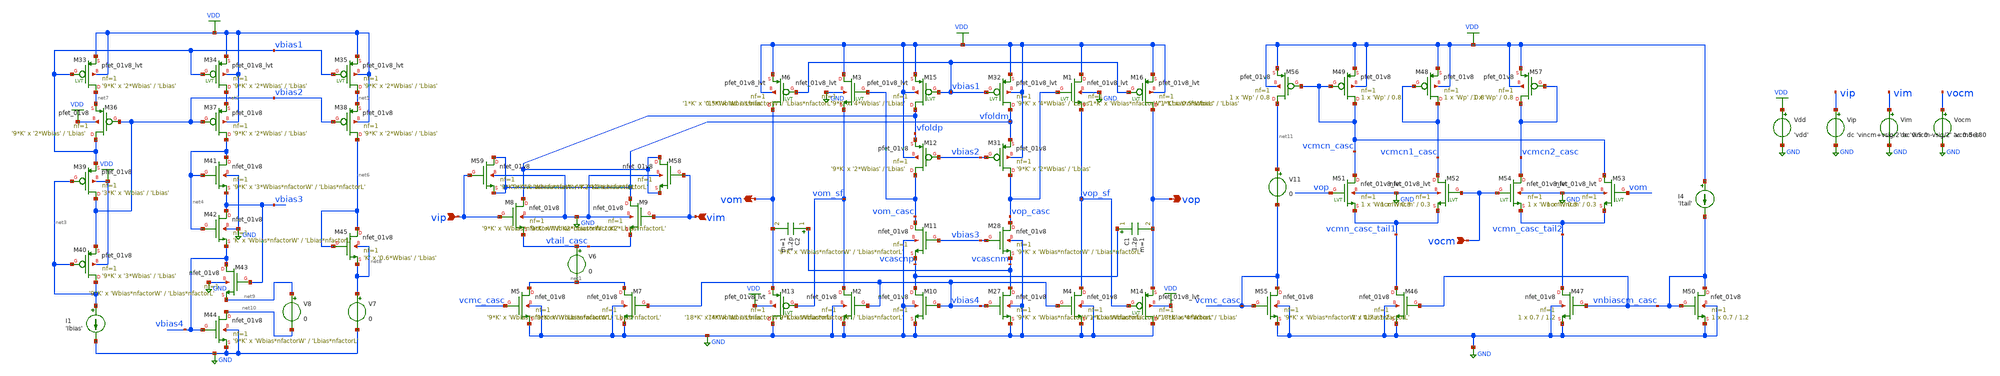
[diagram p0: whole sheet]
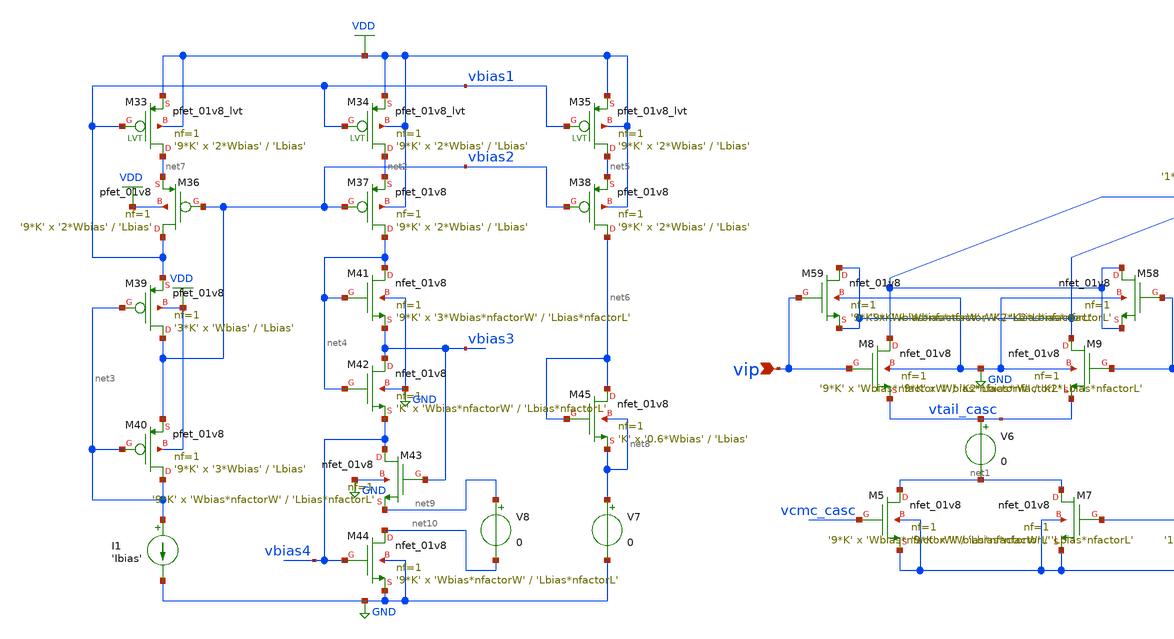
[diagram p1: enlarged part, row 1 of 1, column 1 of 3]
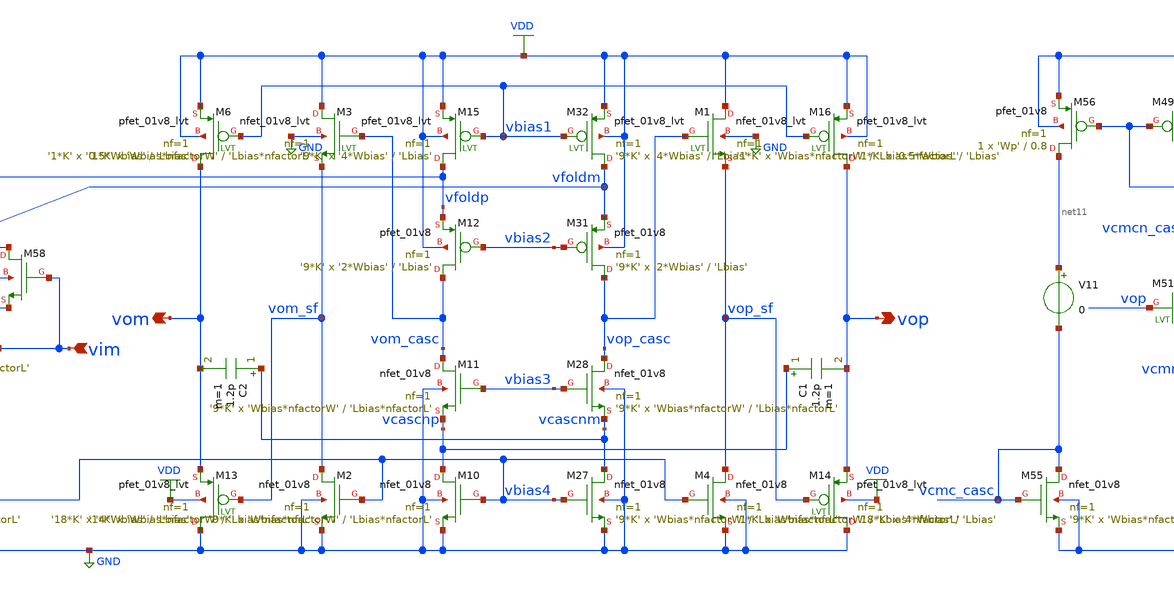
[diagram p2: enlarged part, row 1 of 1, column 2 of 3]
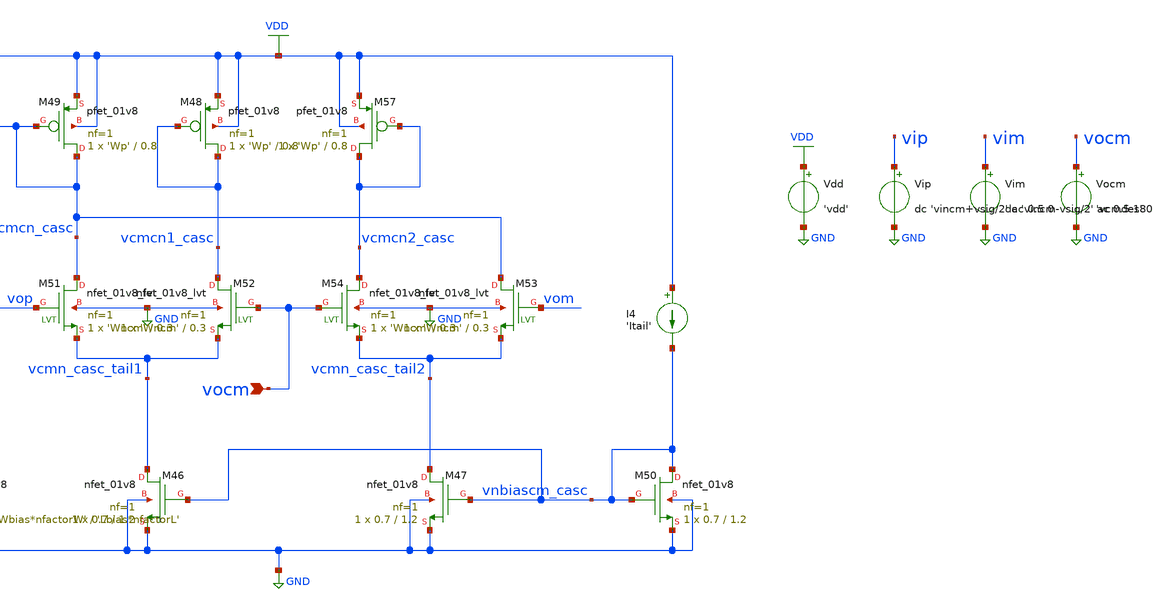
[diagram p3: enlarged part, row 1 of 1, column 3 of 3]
** sch_path: designs/diff_fold_casc_opamp.sch
* Copyright 2020 Stefan Frederik Schippers
* Licensed under the Apache License, Version 2.0 (the "License");
* you may not use this file except in compliance with the License.
* You may obtain a copy of the License at
* https://www.apache.org/licenses/LICENSE-2.0
* Unless required by applicable law or agreed to in writing, software
* distributed under the License is distributed on an "AS IS" BASIS,
* WITHOUT WARRANTIES OR CONDITIONS OF ANY KIND, either express or implied.
* See the License for the specific language governing permissions and
* limitations under the License.
**.subckt diff_fold_casc_opamp vip vim vocm vom vop
*.ipin vip
*.ipin vim
*.ipin vocm
*.opin vom
*.opin vop
Vdd VDD GND 'vdd'
V6 vtail_casc net1 0
XM7 net1 vbias4 GND GND sky130_fd_pr__nfet_01v8 L='Lbias*nfactorL' W='Wbias*nfactorW' nf=1 ad='int((nf+1)/2) * W/nf * 0.29'
+ as='int((nf+2)/2) * W/nf * 0.29' pd='2*int((nf+1)/2) * (W/nf + 0.29)' ps='2*int((nf+2)/2) * (W/nf + 0.29)'
+ nrd='0.29 / W' nrs='0.29 / W' sa=0 sb=0 sd=0 mult='9*K' m='9*K'
XM10 vcascnp vbias4 GND GND sky130_fd_pr__nfet_01v8 L='Lbias*nfactorL' W='Wbias*nfactorW' nf=1 ad='int((nf+1)/2) * W/nf * 0.29'
+ as='int((nf+2)/2) * W/nf * 0.29' pd='2*int((nf+1)/2) * (W/nf + 0.29)' ps='2*int((nf+2)/2) * (W/nf + 0.29)'
+ nrd='0.29 / W' nrs='0.29 / W' sa=0 sb=0 sd=0 mult='9*K' m='9*K'
XM11 vom_casc vbias3 vcascnp GND sky130_fd_pr__nfet_01v8 L='Lbias*nfactorL' W='Wbias*nfactorW' nf=1 ad='int((nf+1)/2) * W/nf * 0.29'
+ as='int((nf+2)/2) * W/nf * 0.29' pd='2*int((nf+1)/2) * (W/nf + 0.29)' ps='2*int((nf+2)/2) * (W/nf + 0.29)'
+ nrd='0.29 / W' nrs='0.29 / W' sa=0 sb=0 sd=0 mult='9*K' m='9*K'
XM27 vcascnm vbias4 GND GND sky130_fd_pr__nfet_01v8 L='Lbias*nfactorL' W='Wbias*nfactorW' nf=1 ad='int((nf+1)/2) * W/nf * 0.29'
+ as='int((nf+2)/2) * W/nf * 0.29' pd='2*int((nf+1)/2) * (W/nf + 0.29)' ps='2*int((nf+2)/2) * (W/nf + 0.29)'
+ nrd='0.29 / W' nrs='0.29 / W' sa=0 sb=0 sd=0 mult='9*K' m='9*K'
XM28 vop_casc vbias3 vcascnm GND sky130_fd_pr__nfet_01v8 L='Lbias*nfactorL' W='Wbias*nfactorW' nf=1 ad='int((nf+1)/2) * W/nf * 0.29'
+ as='int((nf+2)/2) * W/nf * 0.29' pd='2*int((nf+1)/2) * (W/nf + 0.29)' ps='2*int((nf+2)/2) * (W/nf + 0.29)'
+ nrd='0.29 / W' nrs='0.29 / W' sa=0 sb=0 sd=0 mult='9*K' m='9*K'
XM36 vbias1 vbias2 net7 VDD sky130_fd_pr__pfet_01v8 L='Lbias' W='2*Wbias' nf=1 ad='int((nf+1)/2) * W/nf * 0.29'
+ as='int((nf+2)/2) * W/nf * 0.29' pd='2*int((nf+1)/2) * (W/nf + 0.29)' ps='2*int((nf+2)/2) * (W/nf + 0.29)'
+ nrd='0.29 / W' nrs='0.29 / W' sa=0 sb=0 sd=0 mult='9*K' m='9*K'
XM37 net4 vbias2 net2 VDD sky130_fd_pr__pfet_01v8 L='Lbias' W='2*Wbias' nf=1 ad='int((nf+1)/2) * W/nf * 0.29'
+ as='int((nf+2)/2) * W/nf * 0.29' pd='2*int((nf+1)/2) * (W/nf + 0.29)' ps='2*int((nf+2)/2) * (W/nf + 0.29)'
+ nrd='0.29 / W' nrs='0.29 / W' sa=0 sb=0 sd=0 mult='9*K' m='9*K'
XM38 net6 vbias2 net5 VDD sky130_fd_pr__pfet_01v8 L='Lbias' W='2*Wbias' nf=1 ad='int((nf+1)/2) * W/nf * 0.29'
+ as='int((nf+2)/2) * W/nf * 0.29' pd='2*int((nf+1)/2) * (W/nf + 0.29)' ps='2*int((nf+2)/2) * (W/nf + 0.29)'
+ nrd='0.29 / W' nrs='0.29 / W' sa=0 sb=0 sd=0 mult='9*K' m='9*K'
XM39 vbias2 net3 vbias1 VDD sky130_fd_pr__pfet_01v8 L='Lbias' W='Wbias' nf=1 ad='int((nf+1)/2) * W/nf * 0.29'
+ as='int((nf+2)/2) * W/nf * 0.29' pd='2*int((nf+1)/2) * (W/nf + 0.29)' ps='2*int((nf+2)/2) * (W/nf + 0.29)'
+ nrd='0.29 / W' nrs='0.29 / W' sa=0 sb=0 sd=0 mult='3*K' m='3*K'
XM40 net3 net3 vbias2 VDD sky130_fd_pr__pfet_01v8 L='Lbias' W='3*Wbias' nf=1 ad='int((nf+1)/2) * W/nf * 0.29'
+ as='int((nf+2)/2) * W/nf * 0.29' pd='2*int((nf+1)/2) * (W/nf + 0.29)' ps='2*int((nf+2)/2) * (W/nf + 0.29)'
+ nrd='0.29 / W' nrs='0.29 / W' sa=0 sb=0 sd=0 mult='9*K' m='9*K'
XM41 net4 net4 vbias3 GND sky130_fd_pr__nfet_01v8 L='Lbias*nfactorL' W='3*Wbias*nfactorW' nf=1 ad='int((nf+1)/2) * W/nf * 0.29'
+ as='int((nf+2)/2) * W/nf * 0.29' pd='2*int((nf+1)/2) * (W/nf + 0.29)' ps='2*int((nf+2)/2) * (W/nf + 0.29)'
+ nrd='0.29 / W' nrs='0.29 / W' sa=0 sb=0 sd=0 mult='9*K' m='9*K'
XM42 vbias3 net4 vbias4 GND sky130_fd_pr__nfet_01v8 L='Lbias*nfactorL' W='Wbias*nfactorW' nf=1 ad='int((nf+1)/2) * W/nf * 0.29'
+ as='int((nf+2)/2) * W/nf * 0.29' pd='2*int((nf+1)/2) * (W/nf + 0.29)' ps='2*int((nf+2)/2) * (W/nf + 0.29)'
+ nrd='0.29 / W' nrs='0.29 / W' sa=0 sb=0 sd=0 mult='K' m='K'
XM43 vbias4 vbias3 net9 GND sky130_fd_pr__nfet_01v8 L='Lbias*nfactorL' W='Wbias*nfactorW' nf=1 ad='int((nf+1)/2) * W/nf * 0.29'
+ as='int((nf+2)/2) * W/nf * 0.29' pd='2*int((nf+1)/2) * (W/nf + 0.29)' ps='2*int((nf+2)/2) * (W/nf + 0.29)'
+ nrd='0.29 / W' nrs='0.29 / W' sa=0 sb=0 sd=0 mult='9*K' m='9*K'
XM44 net10 vbias4 GND GND sky130_fd_pr__nfet_01v8 L='Lbias*nfactorL' W='Wbias*nfactorW' nf=1 ad='int((nf+1)/2) * W/nf * 0.29'
+ as='int((nf+2)/2) * W/nf * 0.29' pd='2*int((nf+1)/2) * (W/nf + 0.29)' ps='2*int((nf+2)/2) * (W/nf + 0.29)'
+ nrd='0.29 / W' nrs='0.29 / W' sa=0 sb=0 sd=0 mult='9*K' m='9*K'
XM45 net6 net6 net8 net8 sky130_fd_pr__nfet_01v8 L='Lbias' W='0.6*Wbias' nf=1 ad='int((nf+1)/2) * W/nf * 0.29'
+ as='int((nf+2)/2) * W/nf * 0.29' pd='2*int((nf+1)/2) * (W/nf + 0.29)' ps='2*int((nf+2)/2) * (W/nf + 0.29)'
+ nrd='0.29 / W' nrs='0.29 / W' sa=0 sb=0 sd=0 mult='K' m='K'
I1 net3 GND 'Ibias'
V7 net8 GND 0
V8 net9 net10 0
XM8 vfoldp vip vtail_casc GND sky130_fd_pr__nfet_01v8 L='K2*Lbias*nfactorL' W='Wbias*nfactorW' nf=1 ad='int((nf+1)/2) * W/nf * 0.29'
+ as='int((nf+2)/2) * W/nf * 0.29' pd='2*int((nf+1)/2) * (W/nf + 0.29)' ps='2*int((nf+2)/2) * (W/nf + 0.29)'
+ nrd='0.29 / W' nrs='0.29 / W' sa=0 sb=0 sd=0 mult='9*K' m='9*K'
Vip vip GND dc 'vincm+vsig/2' ac 0.5 0
Vim vim GND dc 'vincm-vsig/2' ac 0.5 180
XM46 vcmn_casc_tail1 vnbiascm_casc GND GND sky130_fd_pr__nfet_01v8 L=1.2 W=0.7 nf=1 ad='int((nf+1)/2) * W/nf * 0.29'
+ as='int((nf+2)/2) * W/nf * 0.29' pd='2*int((nf+1)/2) * (W/nf + 0.29)' ps='2*int((nf+2)/2) * (W/nf + 0.29)'
+ nrd='0.29 / W' nrs='0.29 / W' sa=0 sb=0 sd=0 mult=1 m=1
XM47 vcmn_casc_tail2 vnbiascm_casc GND GND sky130_fd_pr__nfet_01v8 L=1.2 W=0.7 nf=1 ad='int((nf+1)/2) * W/nf * 0.29'
+ as='int((nf+2)/2) * W/nf * 0.29' pd='2*int((nf+1)/2) * (W/nf + 0.29)' ps='2*int((nf+2)/2) * (W/nf + 0.29)'
+ nrd='0.29 / W' nrs='0.29 / W' sa=0 sb=0 sd=0 mult=1 m=1
XM48 vcmcn1_casc vcmcn1_casc VDD VDD sky130_fd_pr__pfet_01v8 L=0.8 W='Wp' nf=1 ad='int((nf+1)/2) * W/nf * 0.29'
+ as='int((nf+2)/2) * W/nf * 0.29' pd='2*int((nf+1)/2) * (W/nf + 0.29)' ps='2*int((nf+2)/2) * (W/nf + 0.29)'
+ nrd='0.29 / W' nrs='0.29 / W' sa=0 sb=0 sd=0 mult=1 m=1
XM49 vcmcn_casc vcmcn_casc VDD VDD sky130_fd_pr__pfet_01v8 L=0.8 W='Wp' nf=1 ad='int((nf+1)/2) * W/nf * 0.29'
+ as='int((nf+2)/2) * W/nf * 0.29' pd='2*int((nf+1)/2) * (W/nf + 0.29)' ps='2*int((nf+2)/2) * (W/nf + 0.29)'
+ nrd='0.29 / W' nrs='0.29 / W' sa=0 sb=0 sd=0 mult=1 m=1
I4 VDD vnbiascm_casc 'Itail'
XM50 vnbiascm_casc vnbiascm_casc GND GND sky130_fd_pr__nfet_01v8 L=1.2 W=0.7 nf=1 ad='int((nf+1)/2) * W/nf * 0.29'
+ as='int((nf+2)/2) * W/nf * 0.29' pd='2*int((nf+1)/2) * (W/nf + 0.29)' ps='2*int((nf+2)/2) * (W/nf + 0.29)'
+ nrd='0.29 / W' nrs='0.29 / W' sa=0 sb=0 sd=0 mult=1 m=1
XM51 vcmcn_casc vop vcmn_casc_tail1 GND sky130_fd_pr__nfet_01v8_lvt L=0.3 W='Wncm' nf=1 ad='int((nf+1)/2) * W/nf * 0.29'
+ as='int((nf+2)/2) * W/nf * 0.29' pd='2*int((nf+1)/2) * (W/nf + 0.29)' ps='2*int((nf+2)/2) * (W/nf + 0.29)'
+ nrd='0.29 / W' nrs='0.29 / W' sa=0 sb=0 sd=0 mult=1 m=1
XM52 vcmcn1_casc vocm vcmn_casc_tail1 GND sky130_fd_pr__nfet_01v8_lvt L=0.3 W='Wncm' nf=1 ad='int((nf+1)/2) * W/nf * 0.29'
+ as='int((nf+2)/2) * W/nf * 0.29' pd='2*int((nf+1)/2) * (W/nf + 0.29)' ps='2*int((nf+2)/2) * (W/nf + 0.29)'
+ nrd='0.29 / W' nrs='0.29 / W' sa=0 sb=0 sd=0 mult=1 m=1
XM53 vcmcn_casc vom vcmn_casc_tail2 GND sky130_fd_pr__nfet_01v8_lvt L=0.3 W='Wncm' nf=1 ad='int((nf+1)/2) * W/nf * 0.29'
+ as='int((nf+2)/2) * W/nf * 0.29' pd='2*int((nf+1)/2) * (W/nf + 0.29)' ps='2*int((nf+2)/2) * (W/nf + 0.29)'
+ nrd='0.29 / W' nrs='0.29 / W' sa=0 sb=0 sd=0 mult=1 m=1
XM54 vcmcn2_casc vocm vcmn_casc_tail2 GND sky130_fd_pr__nfet_01v8_lvt L=0.3 W='Wncm' nf=1 ad='int((nf+1)/2) * W/nf * 0.29'
+ as='int((nf+2)/2) * W/nf * 0.29' pd='2*int((nf+1)/2) * (W/nf + 0.29)' ps='2*int((nf+2)/2) * (W/nf + 0.29)'
+ nrd='0.29 / W' nrs='0.29 / W' sa=0 sb=0 sd=0 mult=1 m=1
XM56 net11 vcmcn_casc VDD VDD sky130_fd_pr__pfet_01v8 L=0.8 W='Wp' nf=1 ad='int((nf+1)/2) * W/nf * 0.29'
+ as='int((nf+2)/2) * W/nf * 0.29' pd='2*int((nf+1)/2) * (W/nf + 0.29)' ps='2*int((nf+2)/2) * (W/nf + 0.29)'
+ nrd='0.29 / W' nrs='0.29 / W' sa=0 sb=0 sd=0 mult=1 m=1
XM57 vcmcn2_casc vcmcn2_casc VDD VDD sky130_fd_pr__pfet_01v8 L=0.8 W='Wp' nf=1 ad='int((nf+1)/2) * W/nf * 0.29'
+ as='int((nf+2)/2) * W/nf * 0.29' pd='2*int((nf+1)/2) * (W/nf + 0.29)' ps='2*int((nf+2)/2) * (W/nf + 0.29)'
+ nrd='0.29 / W' nrs='0.29 / W' sa=0 sb=0 sd=0 mult=1 m=1
V11 net11 vcmc_casc 0
Vocm vocm GND 'vcmdes'
XM12 vom_casc vbias2 vfoldp VDD sky130_fd_pr__pfet_01v8 L='Lbias' W='2*Wbias' nf=1 ad='int((nf+1)/2) * W/nf * 0.29'
+ as='int((nf+2)/2) * W/nf * 0.29' pd='2*int((nf+1)/2) * (W/nf + 0.29)' ps='2*int((nf+2)/2) * (W/nf + 0.29)'
+ nrd='0.29 / W' nrs='0.29 / W' sa=0 sb=0 sd=0 mult='9*K' m='9*K'
XM31 vop_casc vbias2 vfoldm VDD sky130_fd_pr__pfet_01v8 L='Lbias' W='2*Wbias' nf=1 ad='int((nf+1)/2) * W/nf * 0.29'
+ as='int((nf+2)/2) * W/nf * 0.29' pd='2*int((nf+1)/2) * (W/nf + 0.29)' ps='2*int((nf+2)/2) * (W/nf + 0.29)'
+ nrd='0.29 / W' nrs='0.29 / W' sa=0 sb=0 sd=0 mult='9*K' m='9*K'
XM15 vfoldp vbias1 VDD VDD sky130_fd_pr__pfet_01v8_lvt L='Lbias' W='4*Wbias' nf=1 ad='int((nf+1)/2) * W/nf * 0.29'
+ as='int((nf+2)/2) * W/nf * 0.29' pd='2*int((nf+1)/2) * (W/nf + 0.29)' ps='2*int((nf+2)/2) * (W/nf + 0.29)'
+ nrd='0.29 / W' nrs='0.29 / W' sa=0 sb=0 sd=0 mult='9*K' m='9*K'
XM32 vfoldm vbias1 VDD VDD sky130_fd_pr__pfet_01v8_lvt L='Lbias' W='4*Wbias' nf=1 ad='int((nf+1)/2) * W/nf * 0.29'
+ as='int((nf+2)/2) * W/nf * 0.29' pd='2*int((nf+1)/2) * (W/nf + 0.29)' ps='2*int((nf+2)/2) * (W/nf + 0.29)'
+ nrd='0.29 / W' nrs='0.29 / W' sa=0 sb=0 sd=0 mult='9*K' m='9*K'
XM33 net7 vbias1 VDD VDD sky130_fd_pr__pfet_01v8_lvt L='Lbias' W='2*Wbias' nf=1 ad='int((nf+1)/2) * W/nf * 0.29'
+ as='int((nf+2)/2) * W/nf * 0.29' pd='2*int((nf+1)/2) * (W/nf + 0.29)' ps='2*int((nf+2)/2) * (W/nf + 0.29)'
+ nrd='0.29 / W' nrs='0.29 / W' sa=0 sb=0 sd=0 mult='9*K' m='9*K'
XM34 net2 vbias1 VDD VDD sky130_fd_pr__pfet_01v8_lvt L='Lbias' W='2*Wbias' nf=1 ad='int((nf+1)/2) * W/nf * 0.29'
+ as='int((nf+2)/2) * W/nf * 0.29' pd='2*int((nf+1)/2) * (W/nf + 0.29)' ps='2*int((nf+2)/2) * (W/nf + 0.29)'
+ nrd='0.29 / W' nrs='0.29 / W' sa=0 sb=0 sd=0 mult='9*K' m='9*K'
XM35 net5 vbias1 VDD VDD sky130_fd_pr__pfet_01v8_lvt L='Lbias' W='2*Wbias' nf=1 ad='int((nf+1)/2) * W/nf * 0.29'
+ as='int((nf+2)/2) * W/nf * 0.29' pd='2*int((nf+1)/2) * (W/nf + 0.29)' ps='2*int((nf+2)/2) * (W/nf + 0.29)'
+ nrd='0.29 / W' nrs='0.29 / W' sa=0 sb=0 sd=0 mult='9*K' m='9*K'
XM5 net1 vcmc_casc GND GND sky130_fd_pr__nfet_01v8 L='Lbias*nfactorL' W='Wbias*nfactorW' nf=1 ad='int((nf+1)/2) * W/nf * 0.29'
+ as='int((nf+2)/2) * W/nf * 0.29' pd='2*int((nf+1)/2) * (W/nf + 0.29)' ps='2*int((nf+2)/2) * (W/nf + 0.29)'
+ nrd='0.29 / W' nrs='0.29 / W' sa=0 sb=0 sd=0 mult='9*K' m='9*K'
XM9 vfoldm vim vtail_casc GND sky130_fd_pr__nfet_01v8 L='K2*Lbias*nfactorL' W='Wbias*nfactorW' nf=1 ad='int((nf+1)/2) * W/nf * 0.29'
+ as='int((nf+2)/2) * W/nf * 0.29' pd='2*int((nf+1)/2) * (W/nf + 0.29)' ps='2*int((nf+2)/2) * (W/nf + 0.29)'
+ nrd='0.29 / W' nrs='0.29 / W' sa=0 sb=0 sd=0 mult='9*K' m='9*K'
XM55 vcmc_casc vcmc_casc GND GND sky130_fd_pr__nfet_01v8 L='Lbias*nfactorL' W='Wbias*nfactorW' nf=1 ad='int((nf+1)/2) * W/nf * 0.29'
+ as='int((nf+2)/2) * W/nf * 0.29' pd='2*int((nf+1)/2) * (W/nf + 0.29)' ps='2*int((nf+2)/2) * (W/nf + 0.29)'
+ nrd='0.29 / W' nrs='0.29 / W' sa=0 sb=0 sd=0 mult='9*K' m='9*K'
XM58 vfoldp vim vfoldp GND sky130_fd_pr__nfet_01v8 L='K2*Lbias*nfactorL' W='Wbias*nfactorW' nf=1 ad='int((nf+1)/2) * W/nf * 0.29'
+ as='int((nf+2)/2) * W/nf * 0.29' pd='2*int((nf+1)/2) * (W/nf + 0.29)' ps='2*int((nf+2)/2) * (W/nf + 0.29)'
+ nrd='0.29 / W' nrs='0.29 / W' sa=0 sb=0 sd=0 mult='9*K' m='9*K'
XM59 vfoldm vip vfoldm GND sky130_fd_pr__nfet_01v8 L='K2*Lbias*nfactorL' W='Wbias*nfactorW' nf=1 ad='int((nf+1)/2) * W/nf * 0.29'
+ as='int((nf+2)/2) * W/nf * 0.29' pd='2*int((nf+1)/2) * (W/nf + 0.29)' ps='2*int((nf+2)/2) * (W/nf + 0.29)'
+ nrd='0.29 / W' nrs='0.29 / W' sa=0 sb=0 sd=0 mult='9*K' m='9*K'
XM2 vom_sf vbias4 GND GND sky130_fd_pr__nfet_01v8 L='Lbias*nfactorL' W='Wbias*nfactorW' nf=1 ad='int((nf+1)/2) * W/nf * 0.29'
+ as='int((nf+2)/2) * W/nf * 0.29' pd='2*int((nf+1)/2) * (W/nf + 0.29)' ps='2*int((nf+2)/2) * (W/nf + 0.29)'
+ nrd='0.29 / W' nrs='0.29 / W' sa=0 sb=0 sd=0 mult='1*K' m='1*K'
XM4 vop_sf vbias4 GND GND sky130_fd_pr__nfet_01v8 L='Lbias*nfactorL' W='Wbias*nfactorW' nf=1 ad='int((nf+1)/2) * W/nf * 0.29'
+ as='int((nf+2)/2) * W/nf * 0.29' pd='2*int((nf+1)/2) * (W/nf + 0.29)' ps='2*int((nf+2)/2) * (W/nf + 0.29)'
+ nrd='0.29 / W' nrs='0.29 / W' sa=0 sb=0 sd=0 mult='1*K' m='1*K'
XM1 VDD vop_casc vop_sf GND sky130_fd_pr__nfet_01v8_lvt L='Lbias*nfactorL' W='Wbias*nfactorW' nf=1 ad='int((nf+1)/2) * W/nf * 0.29'
+ as='int((nf+2)/2) * W/nf * 0.29' pd='2*int((nf+1)/2) * (W/nf + 0.29)' ps='2*int((nf+2)/2) * (W/nf + 0.29)'
+ nrd='0.29 / W' nrs='0.29 / W' sa=0 sb=0 sd=0 mult='1*K' m='1*K'
XM3 VDD vom_casc vom_sf GND sky130_fd_pr__nfet_01v8_lvt L='Lbias*nfactorL' W='Wbias*nfactorW' nf=1 ad='int((nf+1)/2) * W/nf * 0.29'
+ as='int((nf+2)/2) * W/nf * 0.29' pd='2*int((nf+1)/2) * (W/nf + 0.29)' ps='2*int((nf+2)/2) * (W/nf + 0.29)'
+ nrd='0.29 / W' nrs='0.29 / W' sa=0 sb=0 sd=0 mult='1*K' m='1*K'
XM13 GND vom_sf vom VDD sky130_fd_pr__pfet_01v8_lvt L='Lbias' W='4*Wbias' nf=1 ad='int((nf+1)/2) * W/nf * 0.29'
+ as='int((nf+2)/2) * W/nf * 0.29' pd='2*int((nf+1)/2) * (W/nf + 0.29)' ps='2*int((nf+2)/2) * (W/nf + 0.29)'
+ nrd='0.29 / W' nrs='0.29 / W' sa=0 sb=0 sd=0 mult='18*K' m='18*K'
XM14 GND vop_sf vop VDD sky130_fd_pr__pfet_01v8_lvt L='Lbias' W='4*Wbias' nf=1 ad='int((nf+1)/2) * W/nf * 0.29'
+ as='int((nf+2)/2) * W/nf * 0.29' pd='2*int((nf+1)/2) * (W/nf + 0.29)' ps='2*int((nf+2)/2) * (W/nf + 0.29)'
+ nrd='0.29 / W' nrs='0.29 / W' sa=0 sb=0 sd=0 mult='18*K' m='18*K'
XM6 vom vbias1 VDD VDD sky130_fd_pr__pfet_01v8_lvt L='Lbias' W='0.5*Wbias' nf=1 ad='int((nf+1)/2) * W/nf * 0.29'
+ as='int((nf+2)/2) * W/nf * 0.29' pd='2*int((nf+1)/2) * (W/nf + 0.29)' ps='2*int((nf+2)/2) * (W/nf + 0.29)'
+ nrd='0.29 / W' nrs='0.29 / W' sa=0 sb=0 sd=0 mult='1*K' m='1*K'
XM16 vop vbias1 VDD VDD sky130_fd_pr__pfet_01v8_lvt L='Lbias' W='0.5*Wbias' nf=1 ad='int((nf+1)/2) * W/nf * 0.29'
+ as='int((nf+2)/2) * W/nf * 0.29' pd='2*int((nf+1)/2) * (W/nf + 0.29)' ps='2*int((nf+2)/2) * (W/nf + 0.29)'
+ nrd='0.29 / W' nrs='0.29 / W' sa=0 sb=0 sd=0 mult='1*K' m='1*K'
C1 vcascnp vop 1.2p m=1
C2 vcascnm vom 1.2p m=1
**** begin user architecture code

.include $::SKYWATER_MODELS/cells/nfet_01v8/sky130_fd_pr__nfet_01v8__tt.corner.spice
.include $::SKYWATER_MODELS/cells/nfet_01v8_lvt/sky130_fd_pr__nfet_01v8_lvt__tt.corner.spice
.include $::SKYWATER_MODELS/cells/pfet_01v8/sky130_fd_pr__pfet_01v8__tt.corner.spice
.include $::SKYWATER_MODELS/cells/nfet_03v3_nvt/sky130_fd_pr__nfet_03v3_nvt__tt.corner.spice
.include $::SKYWATER_MODELS/cells/nfet_05v0_nvt/sky130_fd_pr__nfet_05v0_nvt__tt.corner.spice
.include $::SKYWATER_MODELS/cells/esd_nfet_01v8/sky130_fd_pr__esd_nfet_01v8__tt.corner.spice
.include $::SKYWATER_MODELS/cells/pfet_01v8_lvt/sky130_fd_pr__pfet_01v8_lvt__tt.corner.spice
.include $::SKYWATER_MODELS/cells/pfet_01v8_hvt/sky130_fd_pr__pfet_01v8_hvt__tt.corner.spice
.include $::SKYWATER_MODELS/cells/esd_pfet_g5v0d10v5/sky130_fd_pr__esd_pfet_g5v0d10v5__tt.corner.spice
.include $::SKYWATER_MODELS/cells/pfet_g5v0d10v5/sky130_fd_pr__pfet_g5v0d10v5__tt.corner.spice
.include $::SKYWATER_MODELS/cells/pfet_g5v0d16v0/sky130_fd_pr__pfet_g5v0d16v0__tt.corner.spice
.include $::SKYWATER_MODELS/cells/nfet_g5v0d10v5/sky130_fd_pr__nfet_g5v0d10v5__tt.corner.spice
.include $::SKYWATER_MODELS/cells/nfet_g5v0d16v0/sky130_fd_pr__nfet_g5v0d16v0__tt_discrete.corner.spice
.include $::SKYWATER_MODELS/cells/esd_nfet_g5v0d10v5/sky130_fd_pr__esd_nfet_g5v0d10v5__tt.corner.spice
.include $::SKYWATER_MODELS/models/corners/tt/nonfet.spice
* Mismatch parameters
.include $::SKYWATER_MODELS/cells/nfet_01v8/sky130_fd_pr__nfet_01v8__mismatch.corner.spice
.include $::SKYWATER_MODELS/cells/pfet_01v8/sky130_fd_pr__pfet_01v8__mismatch.corner.spice
.include $::SKYWATER_MODELS/cells/nfet_01v8_lvt/sky130_fd_pr__nfet_01v8_lvt__mismatch.corner.spice
.include $::SKYWATER_MODELS/cells/pfet_01v8_lvt/sky130_fd_pr__pfet_01v8_lvt__mismatch.corner.spice
.include $::SKYWATER_MODELS/cells/pfet_01v8_hvt/sky130_fd_pr__pfet_01v8_hvt__mismatch.corner.spice
.include $::SKYWATER_MODELS/cells/nfet_g5v0d10v5/sky130_fd_pr__nfet_g5v0d10v5__mismatch.corner.spice
.include $::SKYWATER_MODELS/cells/pfet_g5v0d10v5/sky130_fd_pr__pfet_g5v0d10v5__mismatch.corner.spice
.include $::SKYWATER_MODELS/cells/nfet_05v0_nvt/sky130_fd_pr__nfet_05v0_nvt__mismatch.corner.spice
.include $::SKYWATER_MODELS/cells/nfet_03v3_nvt/sky130_fd_pr__nfet_03v3_nvt__mismatch.corner.spice
* Resistor$::SKYWATER_MODELS/Capacitor
.include $::SKYWATER_MODELS/models/r+c/res_typical__cap_typical.spice
.include $::SKYWATER_MODELS/models/r+c/res_typical__cap_typical__lin.spice
* Special cells
.include $::SKYWATER_MODELS/models/corners/tt/specialized_cells.spice
* All models
.include $::SKYWATER_MODELS/models/all.spice
* Corner
.include $::SKYWATER_MODELS/models/corners/tt/rf.spice

**** end user architecture code
**.ends
.GLOBAL GND
.GLOBAL VDD
**** begin user architecture code

.include diff_fold_casc_opamp_commands.spice

**** end user architecture code
.end
